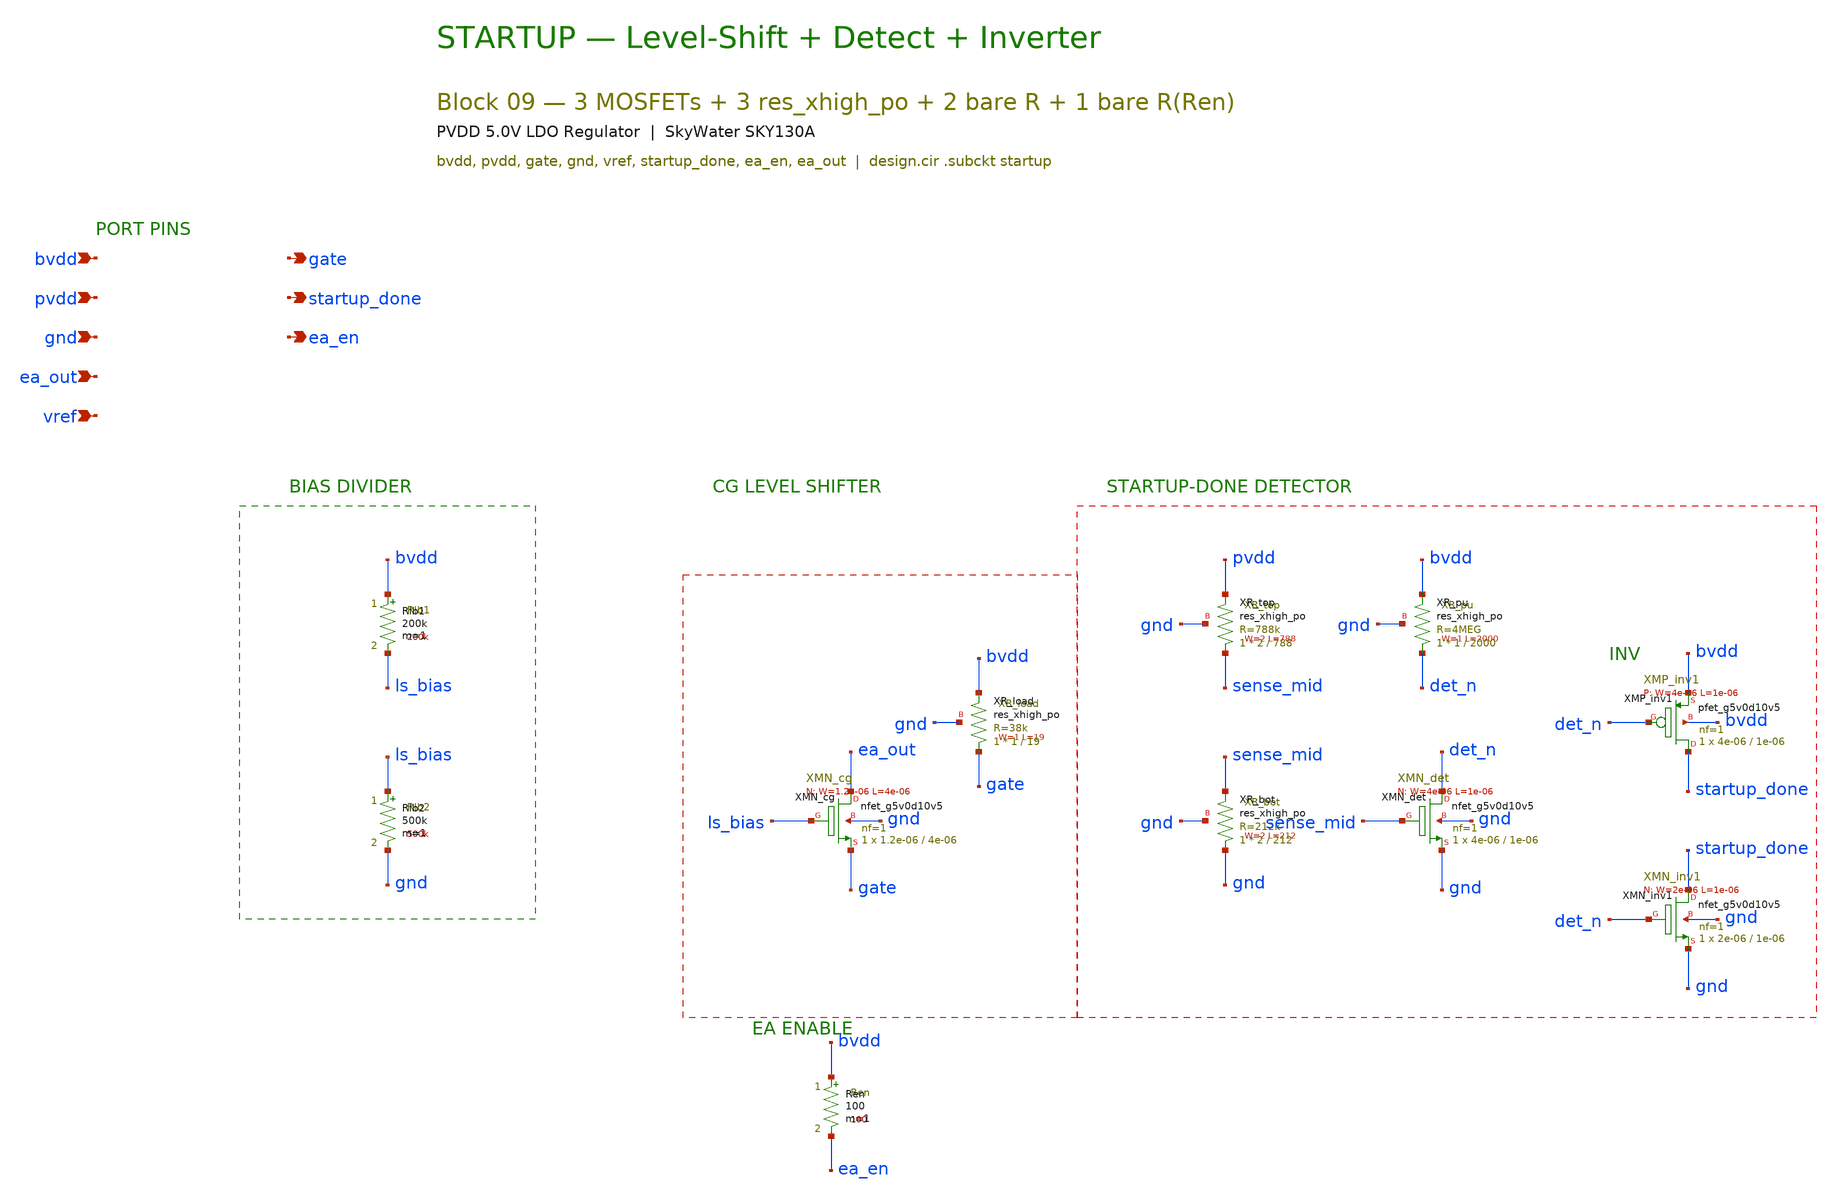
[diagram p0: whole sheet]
** sch_path: pvdd_regulator/10_top_integration/schematics/pvdd_09_startup.sch
**.subckt pvdd_09_startup bvdd pvdd gnd ea_out vref gate startup_done ea_en
*.ipin bvdd
*.ipin pvdd
*.ipin gnd
*.ipin ea_out
*.ipin vref
*.opin gate
*.opin startup_done
*.opin ea_en
Rlb1 bvdd ls_bias 200k m=1
Rlb2 ls_bias gnd 500k m=1
XXMN_cg ea_out ls_bias gate gnd sky130_fd_pr__nfet_g5v0d10v5 L=4e-06 W=1.2e-06 nf=1 ad='int((1 + 1)/2) * 1.2e-06 / 1 * 0.29'
+ as='int((1 + 2)/2) * 1.2e-06 / 1 * 0.29' pd='2*int((1 + 1)/2) * (1.2e-06 / 1 + 0.29)' ps='2*int((1 + 2)/2) * (1.2e-06 / 1 + 0.29)'
+ nrd='0.29 / 1.2e-06 ' nrs='0.29 / 1.2e-06 ' sa=0 sb=0 sd=0 mult=1 m=1
XXR_load gate bvdd gnd sky130_fd_pr__res_xhigh_po W=1 L=19 mult=1 m=1
Ren bvdd ea_en 100 m=1
XXR_top sense_mid pvdd gnd sky130_fd_pr__res_xhigh_po W=2 L=788 mult=1 m=1
XXR_bot gnd sense_mid gnd sky130_fd_pr__res_xhigh_po W=2 L=212 mult=1 m=1
XXMN_det det_n sense_mid gnd gnd sky130_fd_pr__nfet_g5v0d10v5 L=1e-06 W=4e-06 nf=1 ad='int((1 + 1)/2) * 4e-06 / 1 * 0.29'
+ as='int((1 + 2)/2) * 4e-06 / 1 * 0.29' pd='2*int((1 + 1)/2) * (4e-06 / 1 + 0.29)' ps='2*int((1 + 2)/2) * (4e-06 / 1 + 0.29)'
+ nrd='0.29 / 4e-06 ' nrs='0.29 / 4e-06 ' sa=0 sb=0 sd=0 mult=1 m=1
XXR_pu det_n bvdd gnd sky130_fd_pr__res_xhigh_po W=1 L=2000 mult=1 m=1
XXMP_inv1 startup_done det_n bvdd bvdd sky130_fd_pr__pfet_g5v0d10v5 L=1e-06 W=4e-06 nf=1 ad='int((1 + 1)/2) * 4e-06 / 1 * 0.29'
+ as='int((1 + 2)/2) * 4e-06 / 1 * 0.29' pd='2*int((1 + 1)/2) * (4e-06 / 1 + 0.29)' ps='2*int((1 + 2)/2) * (4e-06 / 1 + 0.29)'
+ nrd='0.29 / 4e-06 ' nrs='0.29 / 4e-06 ' sa=0 sb=0 sd=0 mult=1 m=1
XXMN_inv1 startup_done det_n gnd gnd sky130_fd_pr__nfet_g5v0d10v5 L=1e-06 W=2e-06 nf=1 ad='int((1 + 1)/2) * 2e-06 / 1 * 0.29'
+ as='int((1 + 2)/2) * 2e-06 / 1 * 0.29' pd='2*int((1 + 1)/2) * (2e-06 / 1 + 0.29)' ps='2*int((1 + 2)/2) * (2e-06 / 1 + 0.29)'
+ nrd='0.29 / 2e-06 ' nrs='0.29 / 2e-06 ' sa=0 sb=0 sd=0 mult=1 m=1
**.ends
.end
